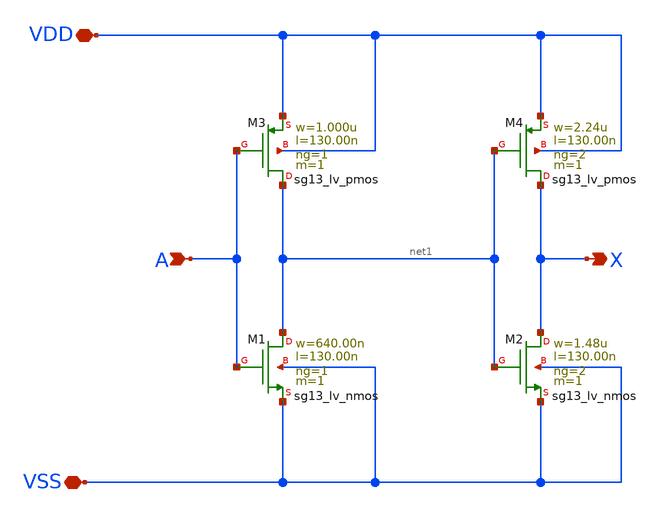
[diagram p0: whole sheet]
** sch_path: ihp-sg13g2/libs.tech/xschem/sg13g2_stdcells/sg13g2_buf_2.sch
**.subckt sg13g2_buf_2 A X VDD VSS
*.ipin A
*.opin X
*.iopin VDD
*.iopin VSS
XM1 net1 A VSS VSS sg13_lv_nmos w=640.00n l=130.00n ng=1 m=1 mm_ok=1
XM2 X net1 VSS VSS sg13_lv_nmos w=1.48u l=130.00n ng=2 m=1 mm_ok=1
XM3 net1 A VDD VDD sg13_lv_pmos w=1.000u l=130.00n ng=1 m=1 mm_ok=1
XM4 X net1 VDD VDD sg13_lv_pmos w=2.24u l=130.00n ng=2 m=1 mm_ok=1
**.ends
.end
